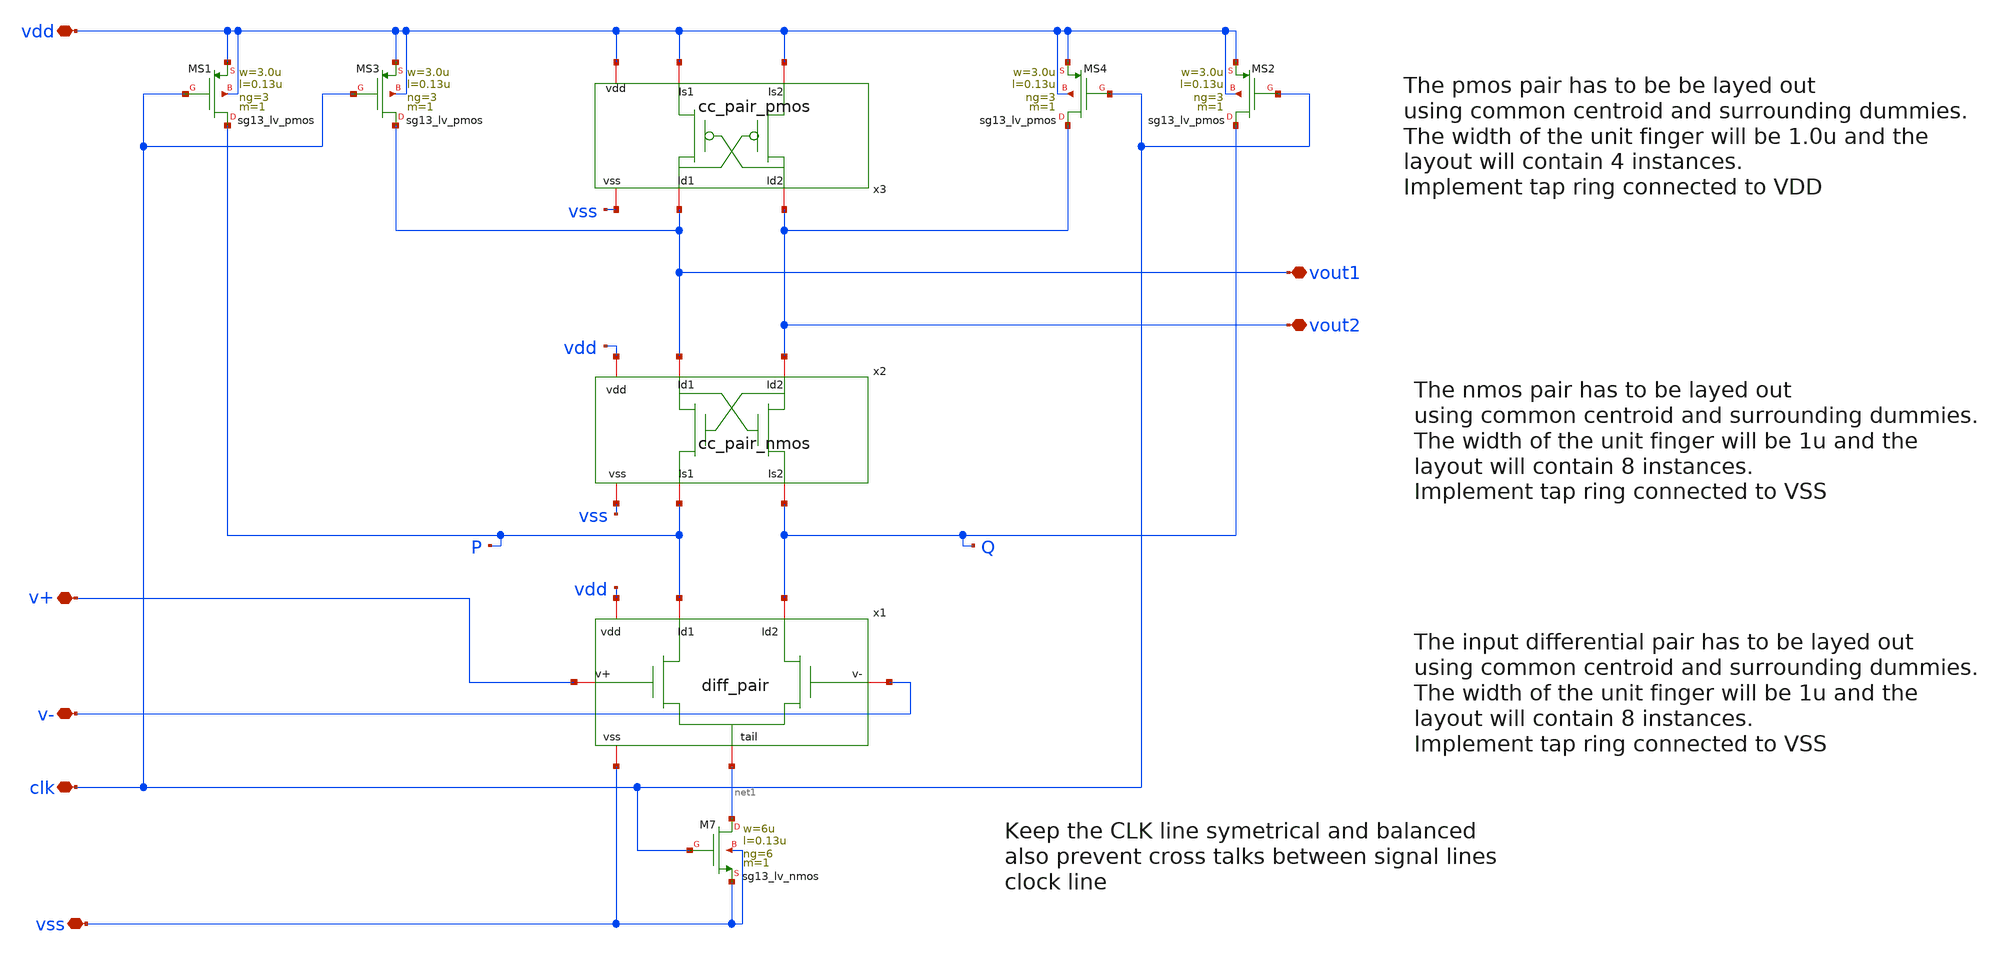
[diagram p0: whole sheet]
** sch_path: CMP7345-main/schematic/xschem/CMP7345-final.sch
**.subckt CMP7345-final v- v+ vss vdd clk vout2 vout1
*.iopin v-
*.iopin v+
*.iopin vss
*.iopin vdd
*.iopin clk
*.iopin vout2
*.iopin vout1
XM7 net1 clk vss vss sg13_lv_nmos w=6u l=0.13u ng=6 m=1 mm_ok=0
XMS4 vout2 clk vdd vdd sg13_lv_pmos w=3.0u l=0.13u ng=3 m=1 mm_ok=0
XMS1 P clk vdd vdd sg13_lv_pmos w=3.0u l=0.13u ng=3 m=1 mm_ok=0
XMS2 Q clk vdd vdd sg13_lv_pmos w=3.0u l=0.13u ng=3 m=1 mm_ok=0
XMS3 vout1 clk vdd vdd sg13_lv_pmos w=3.0u l=0.13u ng=3 m=1 mm_ok=0
x2 vout2 vout1 vss P Q vdd cc_pair_nmos
x3 vout2 vout1 vdd vdd vdd vss cc_pair_pmos
x1 P Q v+ v- vdd net1 vss diff_pair
**.ends

* expanding   symbol:  cc_pair_nmos.sym # of pins=6
** sym_path: CMP7345-main/schematic/xschem/cc_pair_nmos.sym
** sch_path: CMP7345-main/schematic/xschem/cc_pair_nmos.sch
.subckt cc_pair_nmos Id2 Id1 vss Is1 Is2 vdd
*.iopin vss
*.iopin Id2
*.iopin Id1
*.iopin Is2
*.iopin Is1
*.iopin vdd
XMA1 Id1 Id2 Is1 sub! sg13_lv_nmos w=1.0u l=0.26u ng=1 m=1 mm_ok=0
XMA2 Id1 Id2 Is1 sub! sg13_lv_nmos w=1.0u l=0.26u ng=1 m=1 mm_ok=0
XMA3 Id1 Id2 Is1 sub! sg13_lv_nmos w=1.0u l=0.26u ng=1 m=1 mm_ok=0
XMA4 Id1 Id2 Is1 sub! sg13_lv_nmos w=1.0u l=0.26u ng=1 m=1 mm_ok=0
XMB1 Id2 Id1 Is2 sub! sg13_lv_nmos w=1.0u l=0.26u ng=1 m=1 mm_ok=0
XMB2 Id2 Id1 Is2 sub! sg13_lv_nmos w=1.0u l=0.26u ng=1 m=1 mm_ok=0
XMB3 Id2 Id1 Is2 sub! sg13_lv_nmos w=1.0u l=0.26u ng=1 m=1 mm_ok=0
XMB4 Id2 Id1 Is2 sub! sg13_lv_nmos w=1.0u l=0.26u ng=1 m=1 mm_ok=0
XMA5 Id1 Id2 Is1 sub! sg13_lv_nmos w=1.0u l=0.26u ng=1 m=1 mm_ok=0
XMA6 Id1 Id2 Is1 sub! sg13_lv_nmos w=1.0u l=0.26u ng=1 m=1 mm_ok=0
XMA7 Id1 Id2 Is1 sub! sg13_lv_nmos w=1.0u l=0.26u ng=1 m=1 mm_ok=0
XMA8 Id1 Id2 Is1 sub! sg13_lv_nmos w=1.0u l=0.26u ng=1 m=1 mm_ok=0
XMB5 Id2 Id1 Is2 sub! sg13_lv_nmos w=1.0u l=0.26u ng=1 m=1 mm_ok=0
XMB6 Id2 Id1 Is2 sub! sg13_lv_nmos w=1.0u l=0.26u ng=1 m=1 mm_ok=0
XMB7 Id2 Id1 Is2 sub! sg13_lv_nmos w=1.0u l=0.26u ng=1 m=1 mm_ok=0
XMB8 Id2 Id1 Is2 sub! sg13_lv_nmos w=1.0u l=0.26u ng=1 m=1 mm_ok=0
XMA9 vss vss Is1 sub! sg13_lv_nmos w=1.0u l=0.26u ng=1 m=1 mm_ok=0
XMA10 vss vss Is2 sub! sg13_lv_nmos w=1.0u l=0.26u ng=1 m=1 mm_ok=0
XMA11 vss vss Is2 sub! sg13_lv_nmos w=1.0u l=0.26u ng=1 m=1 mm_ok=0
XMA12 vss vss Is1 sub! sg13_lv_nmos w=1.0u l=0.26u ng=1 m=1 mm_ok=0
XMA13 Is1 vss vss sub! sg13_lv_nmos w=1.0u l=0.26u ng=1 m=1 mm_ok=0
XMA14 Is2 vss vss sub! sg13_lv_nmos w=1.0u l=0.26u ng=1 m=1 mm_ok=0
XMA15 Is2 vss vss sub! sg13_lv_nmos w=1.0u l=0.26u ng=1 m=1 mm_ok=0
XMA16 Is1 vss vss sub! sg13_lv_nmos w=1.0u l=0.26u ng=1 m=1 mm_ok=0
XD1 sub! vdd dantenna l=1.0u w=1.0u
XR1 vss sub! ptap1 R=196 w=1.0e-6 l=1.0e-6
.ends


* expanding   symbol:  cc_pair_pmos.sym # of pins=6
** sym_path: CMP7345-main/schematic/xschem/cc_pair_pmos.sym
** sch_path: CMP7345-main/schematic/xschem/cc_pair_pmos.sch
.subckt cc_pair_pmos Id2 Id1 Is2 Is1 vdd vss
*.iopin vdd
*.iopin Id2
*.iopin Id1
*.iopin Is2
*.iopin Is1
*.iopin vss
XMA1 Id1 Id2 Is1 nw sg13_lv_pmos w=1.0u l=0.26u ng=1 m=1 mm_ok=0
XMB1 Id2 Id1 Is2 nw sg13_lv_pmos w=1.0u l=0.26u ng=1 m=1 mm_ok=0
XMA2 Id1 Id2 Is1 nw sg13_lv_pmos w=1.0u l=0.26u ng=1 m=1 mm_ok=0
XMB2 Id2 Id1 Is2 nw sg13_lv_pmos w=1.0u l=0.26u ng=1 m=1 mm_ok=0
XMA3 Id1 Id2 Is1 nw sg13_lv_pmos w=1.0u l=0.26u ng=1 m=1 mm_ok=0
XMA4 Id1 Id2 Is1 nw sg13_lv_pmos w=1.0u l=0.26u ng=1 m=1 mm_ok=0
XMB3 Id2 Id1 Is2 nw sg13_lv_pmos w=1.0u l=0.26u ng=1 m=1 mm_ok=0
XMB4 Id2 Id1 Is2 nw sg13_lv_pmos w=1.0u l=0.26u ng=1 m=1 mm_ok=0
XMD1 vdd vdd vdd nw sg13_lv_pmos w=1.0u l=0.26u ng=1 m=1 mm_ok=0
XMD2 vdd vdd vdd nw sg13_lv_pmos w=1.0u l=0.26u ng=1 m=1 mm_ok=0
XD1 vss nw dpantenna l=0.78u w=0.78u
XR1 vdd nw ntap1 R=262.8 w=0.78e-6 l=0.78e-6
.ends


* expanding   symbol:  diff_pair.sym # of pins=7
** sym_path: CMP7345-main/schematic/xschem/diff_pair.sym
** sch_path: CMP7345-main/schematic/xschem/diff_pair.sch
.subckt diff_pair Id1 Id2 v+ v- vdd tail vss
*.iopin v-
*.iopin v+
*.iopin vss
*.iopin tail
*.iopin Id2
*.iopin Id1
*.iopin vdd
XMA1 Id2 v- tail sub! sg13_lv_nmos w=1.0u l=0.26u ng=1 m=1 mm_ok=0
XMA2 Id2 v- tail sub! sg13_lv_nmos w=1.0u l=0.26u ng=1 m=1 mm_ok=0
XMA3 Id2 v- tail sub! sg13_lv_nmos w=1.0u l=0.26u ng=1 m=1 mm_ok=0
XMA4 Id2 v- tail sub! sg13_lv_nmos w=1.0u l=0.26u ng=1 m=1 mm_ok=0
XMB1 Id1 v+ tail sub! sg13_lv_nmos w=1.0u l=0.26u ng=1 m=1 mm_ok=0
XMB2 Id1 v+ tail sub! sg13_lv_nmos w=1.0u l=0.26u ng=1 m=1 mm_ok=0
XMB3 Id1 v+ tail sub! sg13_lv_nmos w=1.0u l=0.26u ng=1 m=1 mm_ok=0
XMB4 Id1 v+ tail sub! sg13_lv_nmos w=1.0u l=0.26u ng=1 m=1 mm_ok=0
XMA5 Id2 v- tail sub! sg13_lv_nmos w=1.0u l=0.26u ng=1 m=1 mm_ok=0
XMA6 Id2 v- tail sub! sg13_lv_nmos w=1.0u l=0.26u ng=1 m=1 mm_ok=0
XMA7 Id2 v- tail sub! sg13_lv_nmos w=1.0u l=0.26u ng=1 m=1 mm_ok=0
XMA8 Id2 v- tail sub! sg13_lv_nmos w=1.0u l=0.26u ng=1 m=1 mm_ok=0
XMB5 Id1 v+ tail sub! sg13_lv_nmos w=1.0u l=0.26u ng=1 m=1 mm_ok=0
XMB6 Id1 v+ tail sub! sg13_lv_nmos w=1.0u l=0.26u ng=1 m=1 mm_ok=0
XMB7 Id1 v+ tail sub! sg13_lv_nmos w=1.0u l=0.26u ng=1 m=1 mm_ok=0
XMB8 Id1 v+ tail sub! sg13_lv_nmos w=1.0u l=0.26u ng=1 m=1 mm_ok=0
XMA9 vss vss Id2 sub! sg13_lv_nmos w=1.0u l=0.26u ng=1 m=1 mm_ok=0
XMA10 vss vss Id1 sub! sg13_lv_nmos w=1.0u l=0.26u ng=1 m=1 mm_ok=0
XMA11 vss vss Id1 sub! sg13_lv_nmos w=1.0u l=0.26u ng=1 m=1 mm_ok=0
XMA12 vss vss Id2 sub! sg13_lv_nmos w=1.0u l=0.26u ng=1 m=1 mm_ok=0
XMA13 Id2 vss vss sub! sg13_lv_nmos w=1.0u l=0.26u ng=1 m=1 mm_ok=0
XMA14 Id1 vss vss sub! sg13_lv_nmos w=1.0u l=0.26u ng=1 m=1 mm_ok=0
XMA15 Id1 vss vss sub! sg13_lv_nmos w=1.0u l=0.26u ng=1 m=1 mm_ok=0
XMA16 Id2 vss vss sub! sg13_lv_nmos w=1.0u l=0.26u ng=1 m=1 mm_ok=0
XR1 sub! vss ptap1 R=196 w=1.0e-6 l=1.0e-6
XD1 sub! vdd dantenna l=1.0u w=1.0u
.ends

.end
